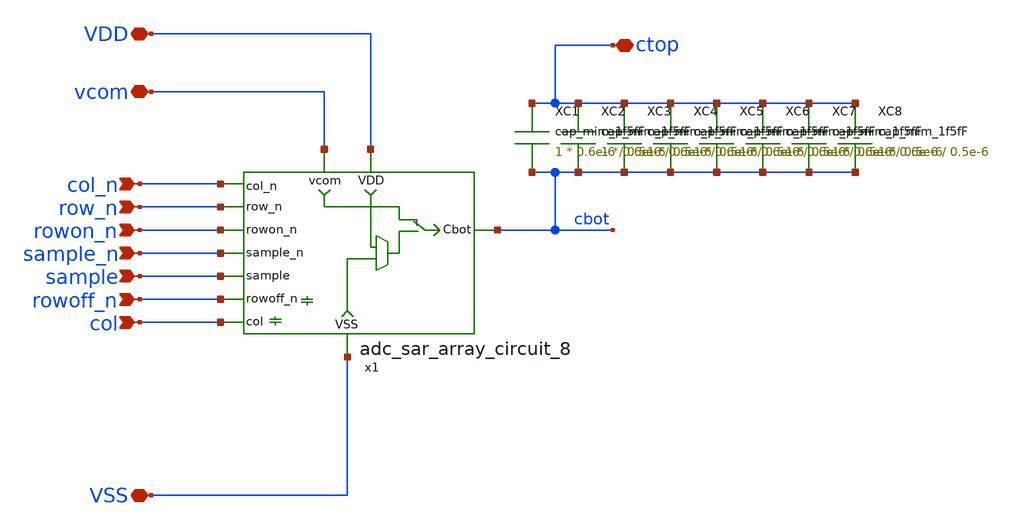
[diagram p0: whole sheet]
** sch_path: adc_sar_wafflecap_8_8.sch
**.subckt adc_sar_wafflecap_8_8 vcom VDD ctop VSS row_n col_n rowon_n sample_n sample rowoff_n col
*.iopin vcom
*.iopin VDD
*.iopin ctop
*.iopin VSS
*.ipin row_n
*.ipin col_n
*.ipin rowon_n
*.ipin sample_n
*.ipin sample
*.ipin rowoff_n
*.ipin col
x1 VDD col_n cbot row_n rowon_n sample_n vcom sample VSS rowoff_n col adc_sar_array_circuit_8
XC1 ctop cbot cap_mim_1f5fF c_width=0.6e-6 c_length=0.5e-6 m=1
XC2 ctop cbot cap_mim_1f5fF c_width=0.6e-6 c_length=0.5e-6 m=1
XC3 ctop cbot cap_mim_1f5fF c_width=0.6e-6 c_length=0.5e-6 m=1
XC4 ctop cbot cap_mim_1f5fF c_width=0.6e-6 c_length=0.5e-6 m=1
XC5 ctop cbot cap_mim_1f5fF c_width=0.6e-6 c_length=0.5e-6 m=1
XC6 ctop cbot cap_mim_1f5fF c_width=0.6e-6 c_length=0.5e-6 m=1
XC7 ctop cbot cap_mim_1f5fF c_width=0.6e-6 c_length=0.5e-6 m=1
XC8 ctop cbot cap_mim_1f5fF c_width=0.6e-6 c_length=0.5e-6 m=1
**.ends

* expanding   symbol:  adc_sar_array_circuit_8.sym # of pins=11
** sym_path: adc_sar_array_circuit_8.sym
** sch_path: adc_sar_array_circuit_8.sch
.subckt adc_sar_array_circuit_8 VDD col_n Cbot row_n rowon_n sample_n vcom sample VSS rowoff_n col
*.ipin sample_n
*.ipin sample
*.iopin vcom
*.ipin col_n
*.ipin row_n
*.ipin rowon_n
*.iopin VDD
*.iopin VSS
*.iopin Cbot
*.ipin col
*.ipin rowoff_n
* noconn col
* noconn rowoff_n
XM1 vdrv sample_n Cbot VSS nfet_03v3 L=0.28u W=0.42u nf=1 ad='int((nf+1)/2) * W/nf * 0.18u' as='int((nf+2)/2) * W/nf * 0.18u'
+ pd='2*int((nf+1)/2) * (W/nf + 0.18u)' ps='2*int((nf+2)/2) * (W/nf + 0.18u)' nrd='0.18u / W' nrs='0.18u / W'
+ sa=0 sb=0 sd=0 m=1
XM2 vcom sample_n Cbot VDD pfet_03v3 L=0.28u W=0.8u nf=1 ad='int((nf+1)/2) * W/nf * 0.18u' as='int((nf+2)/2) * W/nf * 0.18u'
+ pd='2*int((nf+1)/2) * (W/nf + 0.18u)' ps='2*int((nf+2)/2) * (W/nf + 0.18u)' nrd='0.18u / W' nrs='0.18u / W'
+ sa=0 sb=0 sd=0 m=1
XM3 vdrv sample Cbot VDD pfet_03v3 L=0.28u W=0.8u nf=1 ad='int((nf+1)/2) * W/nf * 0.18u' as='int((nf+2)/2) * W/nf * 0.18u'
+ pd='2*int((nf+1)/2) * (W/nf + 0.18u)' ps='2*int((nf+2)/2) * (W/nf + 0.18u)' nrd='0.18u / W' nrs='0.18u / W'
+ sa=0 sb=0 sd=0 m=1
XM4 vcom sample Cbot VSS nfet_03v3 L=0.28u W=0.42u nf=1 ad='int((nf+1)/2) * W/nf * 0.18u' as='int((nf+2)/2) * W/nf * 0.18u'
+ pd='2*int((nf+1)/2) * (W/nf + 0.18u)' ps='2*int((nf+2)/2) * (W/nf + 0.18u)' nrd='0.18u / W' nrs='0.18u / W'
+ sa=0 sb=0 sd=0 m=1
XM5 VDD col_n vint1 VDD pfet_03v3 L=0.28u W=0.8u nf=1 ad='int((nf+1)/2) * W/nf * 0.18u' as='int((nf+2)/2) * W/nf * 0.18u'
+ pd='2*int((nf+1)/2) * (W/nf + 0.18u)' ps='2*int((nf+2)/2) * (W/nf + 0.18u)' nrd='0.18u / W' nrs='0.18u / W'
+ sa=0 sb=0 sd=0 m=1
XM6 vint1 row_n vdrv VDD pfet_03v3 L=0.28u W=0.8u nf=1 ad='int((nf+1)/2) * W/nf * 0.18u' as='int((nf+2)/2) * W/nf * 0.18u'
+ pd='2*int((nf+1)/2) * (W/nf + 0.18u)' ps='2*int((nf+2)/2) * (W/nf + 0.18u)' nrd='0.18u / W' nrs='0.18u / W'
+ sa=0 sb=0 sd=0 m=1
XM7 VDD rowon_n vdrv VDD pfet_03v3 L=0.28u W=0.8u nf=1 ad='int((nf+1)/2) * W/nf * 0.18u' as='int((nf+2)/2) * W/nf * 0.18u'
+ pd='2*int((nf+1)/2) * (W/nf + 0.18u)' ps='2*int((nf+2)/2) * (W/nf + 0.18u)' nrd='0.18u / W' nrs='0.18u / W'
+ sa=0 sb=0 sd=0 m=1
XM8 vint2 rowon_n vdrv VSS nfet_03v3 L=0.28u W=0.42u nf=1 ad='int((nf+1)/2) * W/nf * 0.18u' as='int((nf+2)/2) * W/nf * 0.18u'
+ pd='2*int((nf+1)/2) * (W/nf + 0.18u)' ps='2*int((nf+2)/2) * (W/nf + 0.18u)' nrd='0.18u / W' nrs='0.18u / W'
+ sa=0 sb=0 sd=0 m=1
XM9 VSS col_n vint2 VSS nfet_03v3 L=0.28u W=0.42u nf=1 ad='int((nf+1)/2) * W/nf * 0.18u' as='int((nf+2)/2) * W/nf * 0.18u'
+ pd='2*int((nf+1)/2) * (W/nf + 0.18u)' ps='2*int((nf+2)/2) * (W/nf + 0.18u)' nrd='0.18u / W' nrs='0.18u / W'
+ sa=0 sb=0 sd=0 m=1
XM10 VSS row_n vint2 VSS nfet_03v3 L=0.28u W=0.42u nf=1 ad='int((nf+1)/2) * W/nf * 0.18u' as='int((nf+2)/2) * W/nf * 0.18u'
+ pd='2*int((nf+1)/2) * (W/nf + 0.18u)' ps='2*int((nf+2)/2) * (W/nf + 0.18u)' nrd='0.18u / W' nrs='0.18u / W'
+ sa=0 sb=0 sd=0 m=1
.ends

.end
